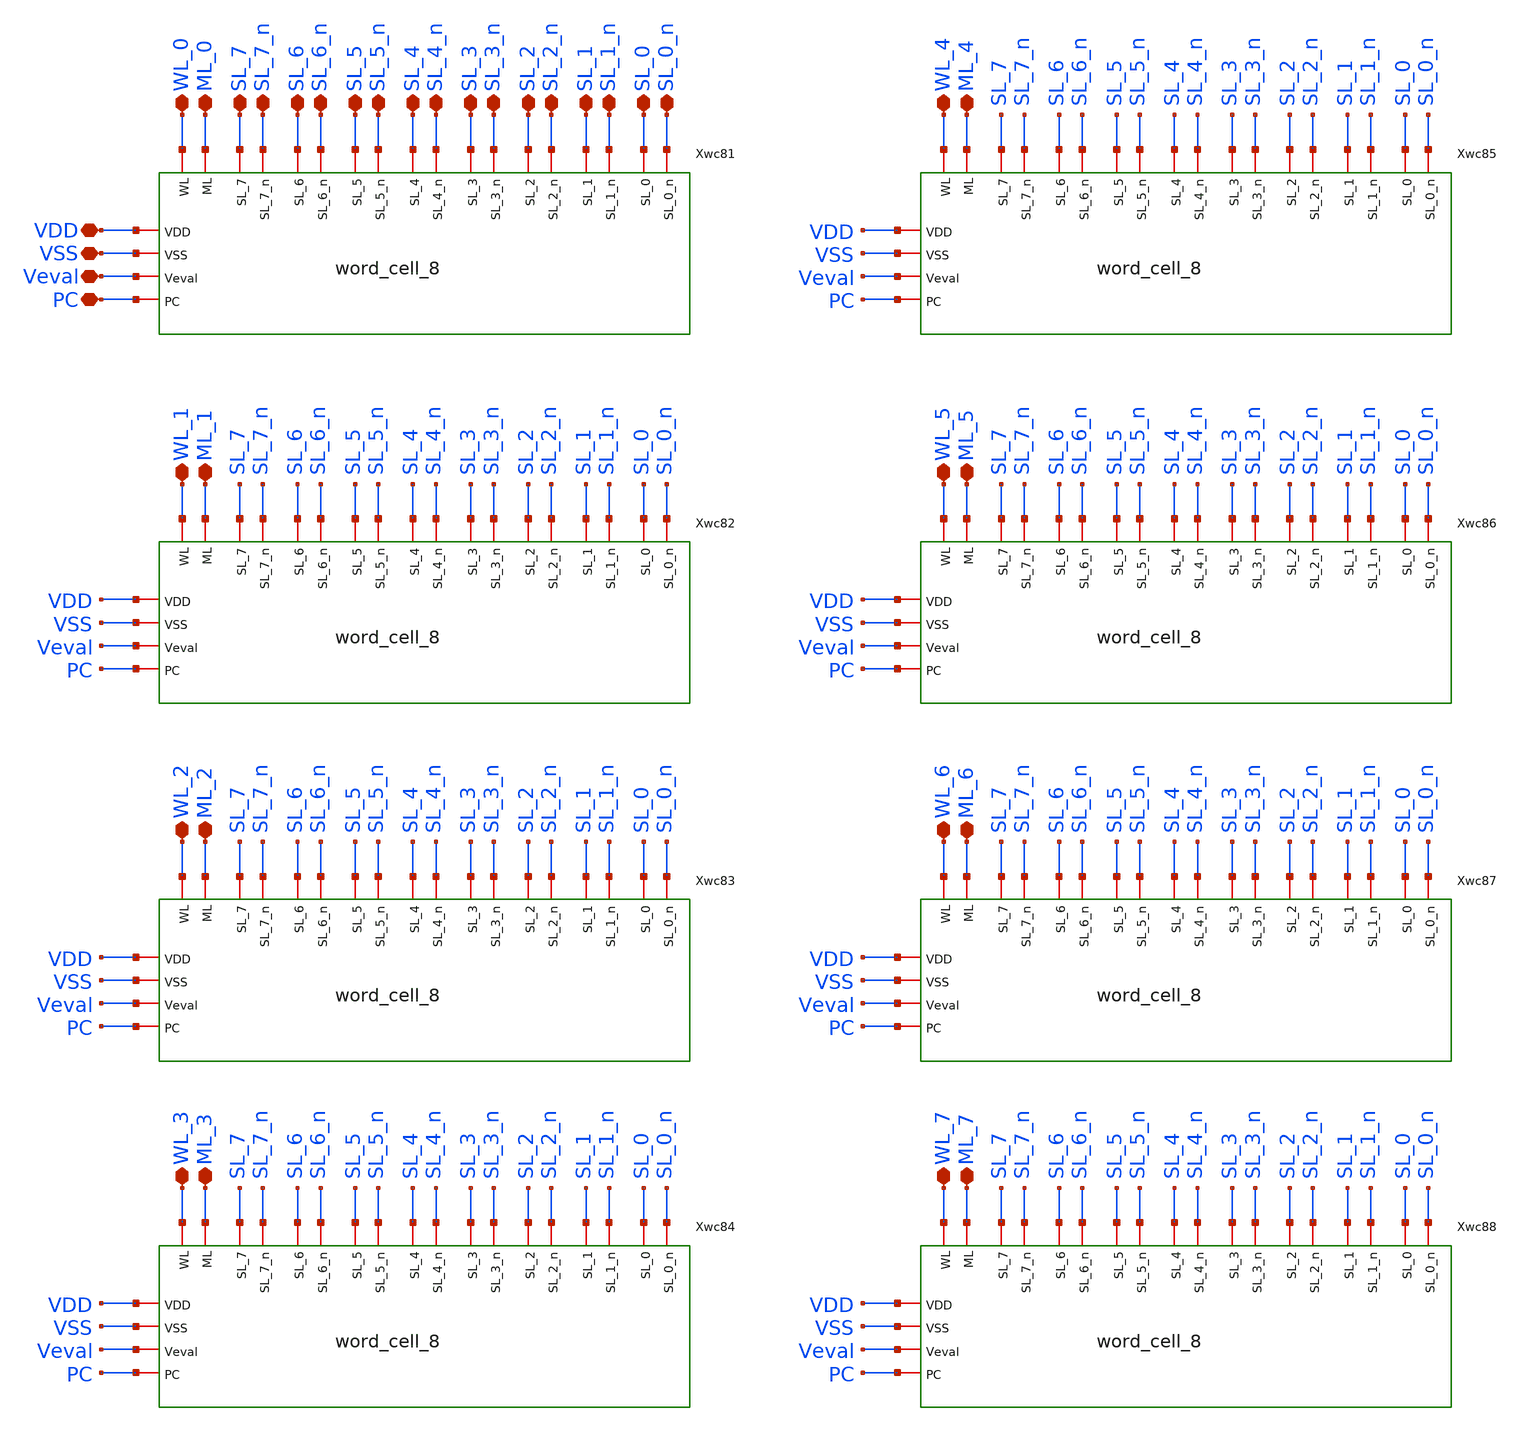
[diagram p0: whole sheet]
** sch_path: xschem/array_8x8.sch
**.subckt array_8x8 WL_0 ML_0 VDD VSS Veval PC WL_1 ML_1 WL_2 ML_2 WL_3 ML_3 WL_4 ML_4 WL_5 ML_5
*+ WL_6 ML_6 WL_7 ML_7 SL_7 SL_7_n SL_6 SL_5 SL_4 SL_3 SL_2 SL_1 SL_0 SL_6_n SL_5_n SL_4_n SL_3_n SL_2_n
*+ SL_1_n SL_0_n
*.iopin WL_0
*.iopin ML_0
*.iopin VDD
*.iopin VSS
*.iopin Veval
*.iopin PC
*.iopin WL_1
*.iopin ML_1
*.iopin WL_2
*.iopin ML_2
*.iopin WL_3
*.iopin ML_3
*.iopin WL_4
*.iopin ML_4
*.iopin WL_5
*.iopin ML_5
*.iopin WL_6
*.iopin ML_6
*.iopin WL_7
*.iopin ML_7
*.iopin SL_7
*.iopin SL_7_n
*.iopin SL_6
*.iopin SL_5
*.iopin SL_4
*.iopin SL_3
*.iopin SL_2
*.iopin SL_1
*.iopin SL_0
*.iopin SL_6_n
*.iopin SL_5_n
*.iopin SL_4_n
*.iopin SL_3_n
*.iopin SL_2_n
*.iopin SL_1_n
*.iopin SL_0_n
Xwc81 SL_3_n SL_1_n SL_2_n SL_0_n SL_7 SL_6 SL_5 SL_4 SL_3 SL_2 SL_1 SL_0 SL_7_n SL_6_n SL_5_n
+ SL_4_n WL_0 ML_0 VDD Veval VSS PC word_cell_8
Xwc82 SL_3_n SL_1_n SL_2_n SL_0_n SL_7 SL_6 SL_5 SL_4 SL_3 SL_2 SL_1 SL_0 SL_7_n SL_6_n SL_5_n
+ SL_4_n WL_1 ML_1 VDD Veval VSS PC word_cell_8
Xwc83 SL_3_n SL_1_n SL_2_n SL_0_n SL_7 SL_6 SL_5 SL_4 SL_3 SL_2 SL_1 SL_0 SL_7_n SL_6_n SL_5_n
+ SL_4_n WL_2 ML_2 VDD Veval VSS PC word_cell_8
Xwc84 SL_3_n SL_1_n SL_2_n SL_0_n SL_7 SL_6 SL_5 SL_4 SL_3 SL_2 SL_1 SL_0 SL_7_n SL_6_n SL_5_n
+ SL_4_n WL_3 ML_3 VDD Veval VSS PC word_cell_8
Xwc85 SL_3_n SL_1_n SL_2_n SL_0_n SL_7 SL_6 SL_5 SL_4 SL_3 SL_2 SL_1 SL_0 SL_7_n SL_6_n SL_5_n
+ SL_4_n WL_4 ML_4 VDD Veval VSS PC word_cell_8
Xwc86 SL_3_n SL_1_n SL_2_n SL_0_n SL_7 SL_6 SL_5 SL_4 SL_3 SL_2 SL_1 SL_0 SL_7_n SL_6_n SL_5_n
+ SL_4_n WL_5 ML_5 VDD Veval VSS PC word_cell_8
Xwc87 SL_3_n SL_1_n SL_2_n SL_0_n SL_7 SL_6 SL_5 SL_4 SL_3 SL_2 SL_1 SL_0 SL_7_n SL_6_n SL_5_n
+ SL_4_n WL_6 ML_6 VDD Veval VSS PC word_cell_8
Xwc88 SL_3_n SL_1_n SL_2_n SL_0_n SL_7 SL_6 SL_5 SL_4 SL_3 SL_2 SL_1 SL_0 SL_7_n SL_6_n SL_5_n
+ SL_4_n WL_7 ML_7 VDD Veval VSS PC word_cell_8
**.ends

* expanding   symbol:  /home/designer/shared/word_cell_8.sym # of pins=22
** sym_path: xschem/word_cell_8.sym
** sch_path: xschem/word_cell_8.sch
.subckt word_cell_8 SL_3_n SL_1_n SL_2_n SL_0_n SL_7 SL_6 SL_5 SL_4 SL_3 SL_2 SL_1 SL_0 SL_7_n
+ SL_6_n SL_5_n SL_4_n WL ML VDD Veval VSS PC
*.iopin VSS
*.iopin Veval
*.iopin VDD
*.iopin WL
*.iopin ML
*.iopin SL_7
*.iopin SL_6
*.iopin SL_5
*.iopin SL_4
*.iopin SL_3
*.iopin SL_2
*.iopin SL_1
*.iopin SL_0
*.iopin SL_7_n
*.iopin SL_6_n
*.iopin SL_5_n
*.iopin SL_4_n
*.iopin SL_3_n
*.iopin SL_2_n
*.iopin SL_1_n
*.iopin SL_0_n
*.ipin PC
Xbc1 WL SL_7 SL_7_n VDD ML Veval VSS bitcell
Xbc2 WL SL_6 SL_6_n VDD ML Veval VSS bitcell
Xbc3 WL SL_5 SL_5_n VDD ML Veval VSS bitcell
Xbc4 WL SL_4 SL_4_n VDD ML Veval VSS bitcell
Xbc5 WL SL_3 SL_3_n VDD ML Veval VSS bitcell
Xbc6 WL SL_2 SL_2_n VDD ML Veval VSS bitcell
Xbc7 WL SL_1 SL_1_n VDD ML Veval VSS bitcell
Xbc8 WL SL_0 SL_0_n VDD ML Veval VSS bitcell
XMP0 ML PC VDD VDD sg13_lv_pmos w=2.24u l=130.00n ng=1 m=1 mm_ok=1
.ends


* expanding   symbol:  /home/designer/shared/bitcell.sym # of pins=7
** sym_path: xschem/bitcell.sym
** sch_path: xschem/bitcell.sch
.subckt bitcell WL SL SL_n VDD ML Veval VSS
*.ipin SL
*.ipin SL_n
*.ipin WL
*.iopin ML
*.ipin Veval
*.iopin VDD
*.iopin VSS
XMN1 SL WL D_n VSS sg13_lv_nmos w=740.00n l=130.00n ng=1 m=1 mm_ok=1
XMN2 SL_n WL D VSS sg13_lv_nmos w=740.00n l=130.00n ng=1 m=1 mm_ok=1
XMN3 net1 D_n SL VSS sg13_lv_nmos w=740.00n l=130.00n ng=1 m=1 mm_ok=1
XMN4 net1 D SL_n VSS sg13_lv_nmos w=740.00n l=130.00n ng=1 m=1 mm_ok=1
XMN5 ML net1 net2 VSS sg13_lv_nmos w=740.00n l=130.00n ng=1 m=1 mm_ok=1
XMN6 net2 Veval VSS VSS sg13_lv_nmos w=740.00n l=130.00n ng=1 m=1 mm_ok=1
X1 VDD D D_n VSS my_inv
X2 VDD D_n D VSS my_inv
.ends


* expanding   symbol:  /home/designer/shared/my_inv.sym # of pins=4
** sym_path: xschem/my_inv.sym
** sch_path: xschem/my_inv.sch
.subckt my_inv VDD Y A VSS
*.opin Y
*.ipin A
*.iopin VDD
*.iopin VSS
XMN0 Y A VSS VSS sg13_lv_nmos w=740.00n l=130.00n ng=1 m=1 mm_ok=1
XMP0 Y A VDD VDD sg13_lv_pmos w=1.12u l=130.00n ng=1 m=1 mm_ok=1
.ends

.end
